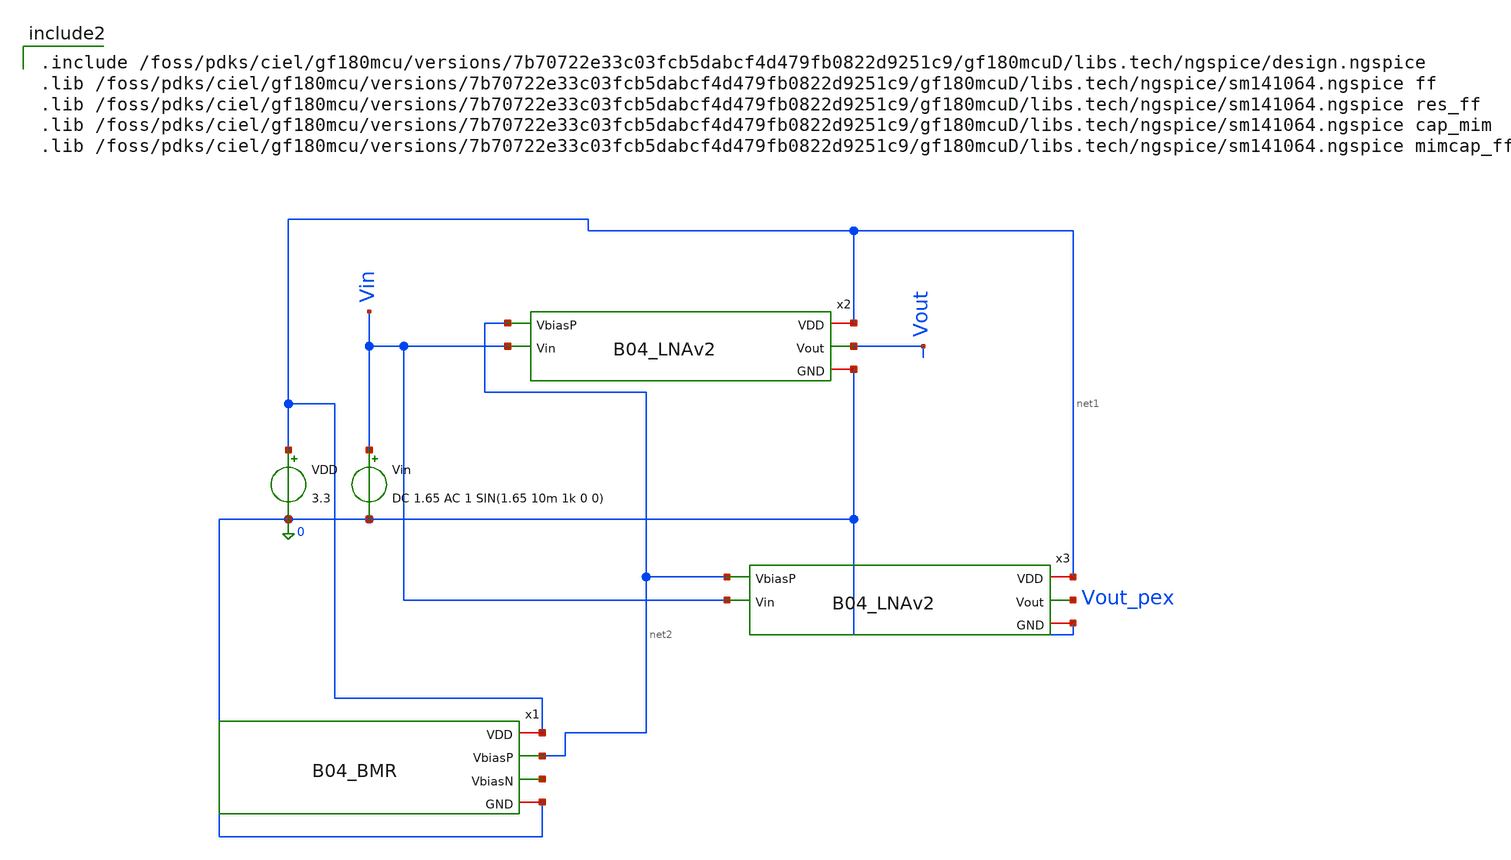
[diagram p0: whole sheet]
** sch_path: analog/B04_tb_LNAv2.sch
**.subckt B04_tb_LNAv2
VDD net1 0 3.3
Vin Vin 0 DC 1.65 AC 1 SIN(1.65 10m 1k 0 0)
x1 net1 net2 net3 0 B04_BMR
x2 net1 net2 Vout Vin 0 B04_LNAv2
x3 net1 net2 Vout_pex Vin 0 B04_LNAv2
**** begin user architecture code


.control
set color0=white
set color1=black
set xbrushwidth=2

echo =================================================
echo 1. DC OPERATING POINT ANALYSIS
echo =================================================
op
print v(vout)
print v(x2.net1)
print @m.x2.xm1.m0[gm]
print @m.x2.xm1.m0[gds]
print @m.x2.xm2.m0[gm]
print @m.x2.xm2.m0[gds]
print @m.x2.xm3.m0[gds]
print @m.x2.xm4.m0[gds]

echo Arus PMOS LNA (M1):
print @m.x2.xm1.m0[id]
echo Arus Penguat Utama NMOS LNA (M2):
print @m.x2.xm2.m0[id]

echo =================================================
echo 2. AC ANALYSIS
echo =================================================
ac dec 50 1 100meg

meas ac peak_gain MAX vdb(vout)
let minus3db = peak_gain - 3
meas ac f_low WHEN vdb(vout)=minus3db RISE=1
meas ac f_high WHEN vdb(vout)=minus3db FALL=1

plot vdb(vout) ylabel 'Gain (dB)' xlabel 'Frequency (Hz)' title 'LNA AC Response'
plot cph(vout)*180/pi ylabel 'Phase (Deg)' xlabel 'Frequency (Hz)' title 'LNA Phase Response'

echo =================================================
echo 3. TRANSIENT ANALYSIS
echo =================================================
tran 10u 5m
plot v(vout) v(Vin) ylabel 'Voltage (V)' xlabel 'Time (s)' title 'Transient Response (1mVp 1kHz)'

echo =================================================
echo 4. NOISE ANALYSIS
echo =================================================
noise v(vout) Vin dec 20 1k 8k
setplot noise1
print onoise_total inoise_total
plot inoise_spectrum ylabel 'V/sqrt(Hz)' xlabel 'Frequency (Hz)' title 'Input Referred Noise'
plot onoise_spectrum ylabel 'V/sqrt(Hz)' xlabel 'Frequency (Hz)' title 'Output Referred Noise'
.endc



.include /foss/pdks/ciel/gf180mcu/versions/7b70722e33c03fcb5dabcf4d479fb0822d9251c9/gf180mcuD/libs.tech/ngspice/design.ngspice
.lib /foss/pdks/ciel/gf180mcu/versions/7b70722e33c03fcb5dabcf4d479fb0822d9251c9/gf180mcuD/libs.tech/ngspice/sm141064.ngspice ff
.lib /foss/pdks/ciel/gf180mcu/versions/7b70722e33c03fcb5dabcf4d479fb0822d9251c9/gf180mcuD/libs.tech/ngspice/sm141064.ngspice res_ff
.lib /foss/pdks/ciel/gf180mcu/versions/7b70722e33c03fcb5dabcf4d479fb0822d9251c9/gf180mcuD/libs.tech/ngspice/sm141064.ngspice cap_mim
.lib /foss/pdks/ciel/gf180mcu/versions/7b70722e33c03fcb5dabcf4d479fb0822d9251c9/gf180mcuD/libs.tech/ngspice/sm141064.ngspice mimcap_ff

**** end user architecture code
**.ends
.end
